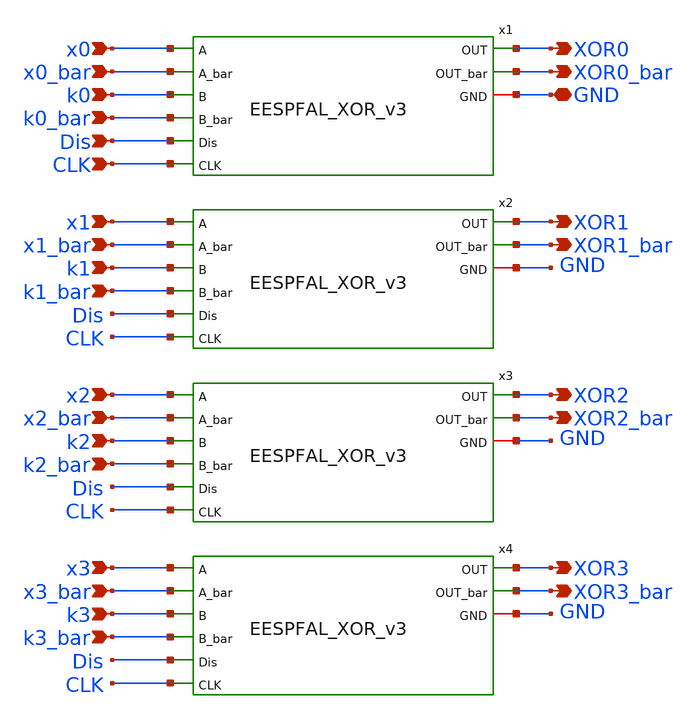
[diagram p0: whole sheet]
** sch_path: skywater_stuff/EESPFAL_4in_XOR_flat.sch
**.subckt EESPFAL_4in_XOR_flat x0 x0_bar k0 k0_bar x1 x1_bar k1 k1_bar x2 x2_bar k2 k2_bar x3 x3_bar
*+ k3 k3_bar XOR0_bar XOR0 XOR1_bar XOR1 XOR2_bar XOR2 XOR3_bar XOR3 GND Dis CLK
*.ipin x0
*.ipin x0_bar
*.ipin k0
*.ipin k0_bar
*.ipin x1
*.ipin x1_bar
*.ipin k1
*.ipin k1_bar
*.ipin x2
*.ipin x2_bar
*.ipin k2
*.ipin k2_bar
*.ipin x3
*.ipin x3_bar
*.ipin k3
*.ipin k3_bar
*.opin XOR0_bar
*.opin XOR0
*.opin XOR1_bar
*.opin XOR1
*.opin XOR2_bar
*.opin XOR2
*.opin XOR3_bar
*.opin XOR3
*.iopin GND
*.ipin Dis
*.ipin CLK
x2 x1 x1_bar k1 k1_bar XOR1 XOR1_bar Dis GND CLK EESPFAL_XOR_v3
x4 x3 x3_bar k3 k3_bar XOR3 XOR3_bar Dis GND CLK EESPFAL_XOR_v3
x3 x2 x2_bar k2 k2_bar XOR2 XOR2_bar Dis GND CLK EESPFAL_XOR_v3
x1 x0 x0_bar k0 k0_bar XOR0 XOR0_bar Dis GND CLK EESPFAL_XOR_v3
**.ends
.end
